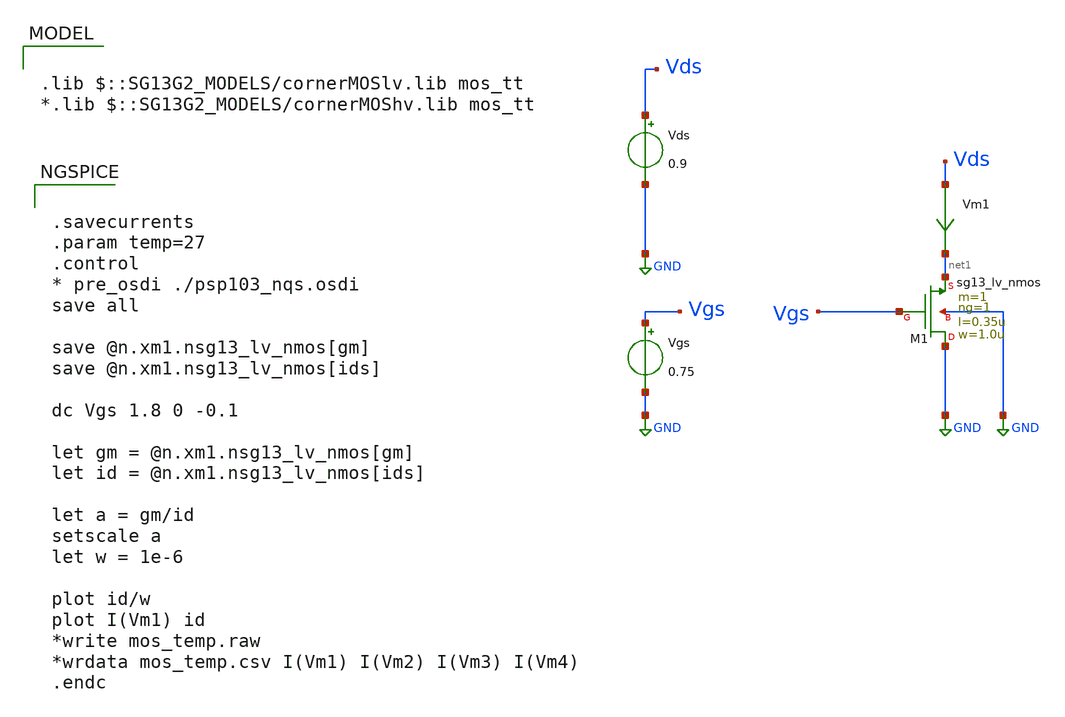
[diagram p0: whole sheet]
** sch_path: ihp_lv_nmos.sch
**.subckt ihp_lv_nmos
Vgs Vgs GND 0.75
Vds Vds GND 0.9
XM1 GND Vgs net1 GND sg13_lv_nmos w=1.0u l=0.35u ng=1 m=1 mm_ok=1
Vm1 Vds net1 0
.save i(vm1)
**** begin user architecture code

.lib $::SG13G2_MODELS/cornerMOSlv.lib mos_tt
*.lib $::SG13G2_MODELS/cornerMOShv.lib mos_tt



.savecurrents
.param temp=27
.control
* pre_osdi ./psp103_nqs.osdi
save all

save @n.xm1.nsg13_lv_nmos[gm]
save @n.xm1.nsg13_lv_nmos[ids]

dc Vgs 1.8 0 -0.1

let gm = @n.xm1.nsg13_lv_nmos[gm]
let id = @n.xm1.nsg13_lv_nmos[ids]

let a = gm/id
setscale a
let w = 1e-6

plot id/w
plot I(Vm1) id
*write mos_temp.raw
*wrdata mos_temp.csv I(Vm1) I(Vm2) I(Vm3) I(Vm4)
.endc



**** end user architecture code
**.ends
.GLOBAL GND
.end
